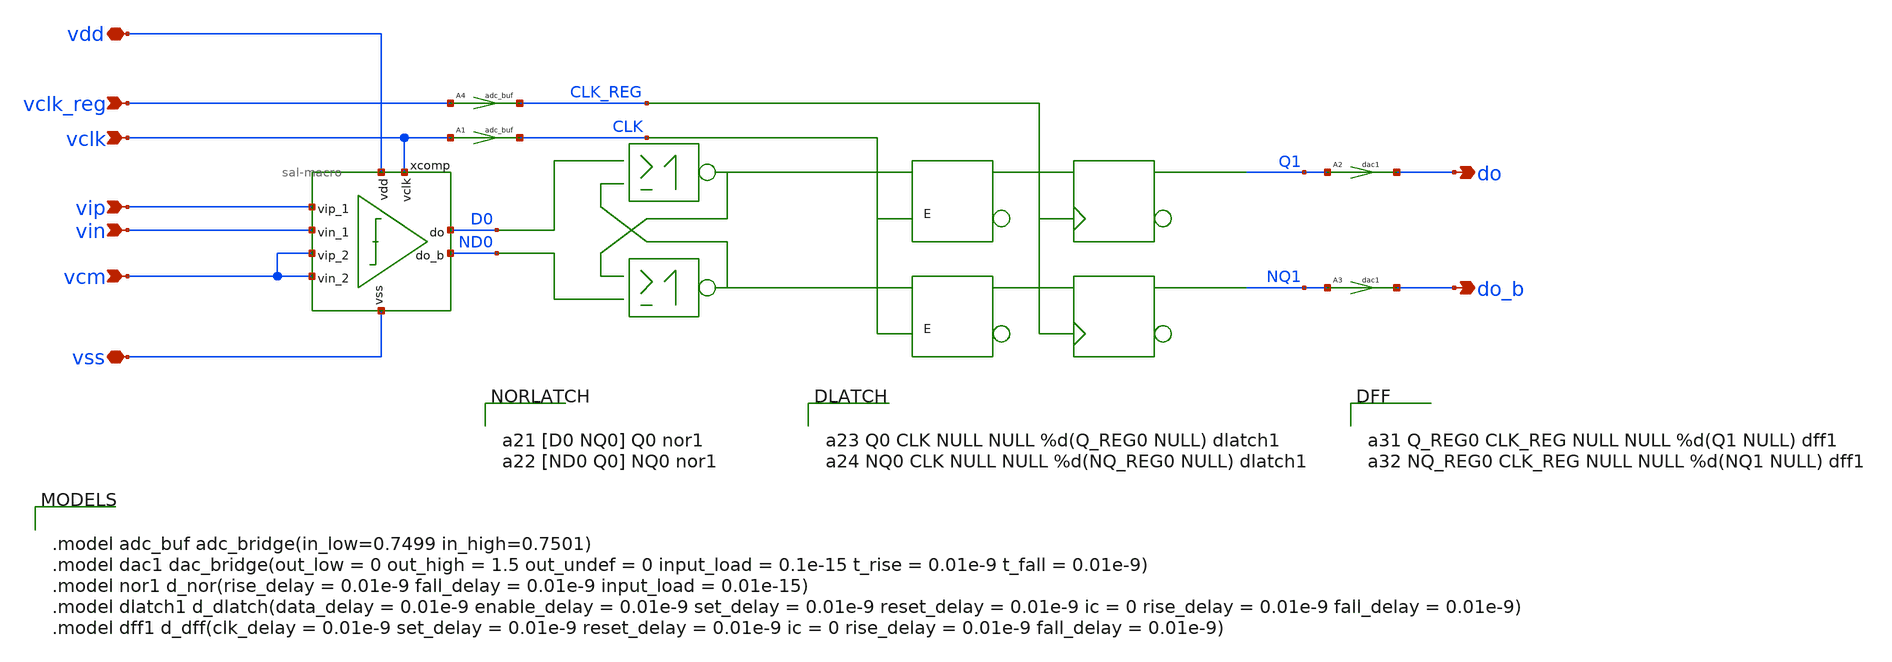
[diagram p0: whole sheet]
** sch_path: xschem/legacy/adc-1b-ideal.sch
**.subckt adc-1b-ideal vss vip vin vcm vclk do_b do vdd vclk_reg
*.iopin vss
*.ipin vip
*.ipin vin
*.ipin vcm
*.ipin vclk
*.opin do_b
*.opin do
*.iopin vdd
*.ipin vclk_reg
A3 [ NQ1 ] [ do_b ] dac1
A2 [ Q1 ] [ do ] dac1
xcomp vdd vclk ND0 D0 vin vcm vcm vip vss sal-macro
A1 [ vclk ] [ CLK ] adc_buf
A4 [ vclk_reg ] [ CLK_REG ] adc_buf
**.ends

* expanding   symbol:  sal-macro.sym # of pins=9
** sym_path: xschem/sal-macro.sym
** sch_path: xschem/sal-macro.sch
.subckt sal-macro vdd vclk do_b do vin_1 vip_2 vin_2 vip_1 vss
*.iopin vss
*.ipin vip_1
*.ipin vip_2
*.ipin vin_2
*.opin do
*.ipin vin_1
*.iopin vdd
*.opin do_b
*.ipin vclk
A1 [ net5 ] [ do ] comp0
G1 net2 net1 vip_1 net1 10e-6
**** begin user architecture code

.model comp0 adc_bridge(in_low=0.74 in_high=0.76)

**** end user architecture code
G3 net3 net1 vin_1 net1 10e-6
S1 net1 vss vclk vss SW1
G2 net5 net3 net4 net3 10e-6
G4 net4 net2 net5 net2 10e-6
G5 vdd net5 vdd net4 10e-6
G6 vdd net4 vdd net5 10e-6
S3 vdd net4 vdd vclk SW1
S4 vdd net2 vdd vclk SW1
S5 vdd net5 vdd vclk SW1
S6 vdd net2 vdd vclk SW1
A2 [ net4 ] [ do_b ] comp0
R1 vdd net4 1Meg m=1
R2 vdd net5 1Meg m=1
R3 net5 net3 1Meg m=1
R4 net4 net2 1Meg m=1
R5 net2 net1 100Meg m=1
R6 net3 net1 100e-6 m=1
.ends

**** begin user architecture code


.model adc_buf adc_bridge(in_low=0.7499 in_high=0.7501)
.model dac1 dac_bridge(out_low = 0 out_high = 1.5 out_undef = 0 input_load = 0.1e-15 t_rise =
+ 0.01e-9 t_fall = 0.01e-9)
.model nor1 d_nor(rise_delay = 0.01e-9 fall_delay = 0.01e-9 input_load = 0.01e-15)
.model dlatch1 d_dlatch(data_delay = 0.01e-9 enable_delay = 0.01e-9 set_delay = 0.01e-9 reset_delay
+ = 0.01e-9 ic = 0 rise_delay = 0.01e-9 fall_delay = 0.01e-9)
.model dff1 d_dff(clk_delay = 0.01e-9 set_delay = 0.01e-9 reset_delay = 0.01e-9 ic = 0 rise_delay =
+ 0.01e-9 fall_delay = 0.01e-9)




a21 [D0 NQ0] Q0 nor1
a22 [ND0 Q0] NQ0 nor1




a23 Q0 CLK NULL NULL %d(Q_REG0 NULL) dlatch1
a24 NQ0 CLK NULL NULL %d(NQ_REG0 NULL) dlatch1




a31 Q_REG0 CLK_REG NULL NULL %d(Q1 NULL) dff1
a32 NQ_REG0 CLK_REG NULL NULL %d(NQ1 NULL) dff1


.MODEL SW1 SW( VT=0.75 VH=0.01 RON=1 ROFF=100Meg )
**** end user architecture code
.end
